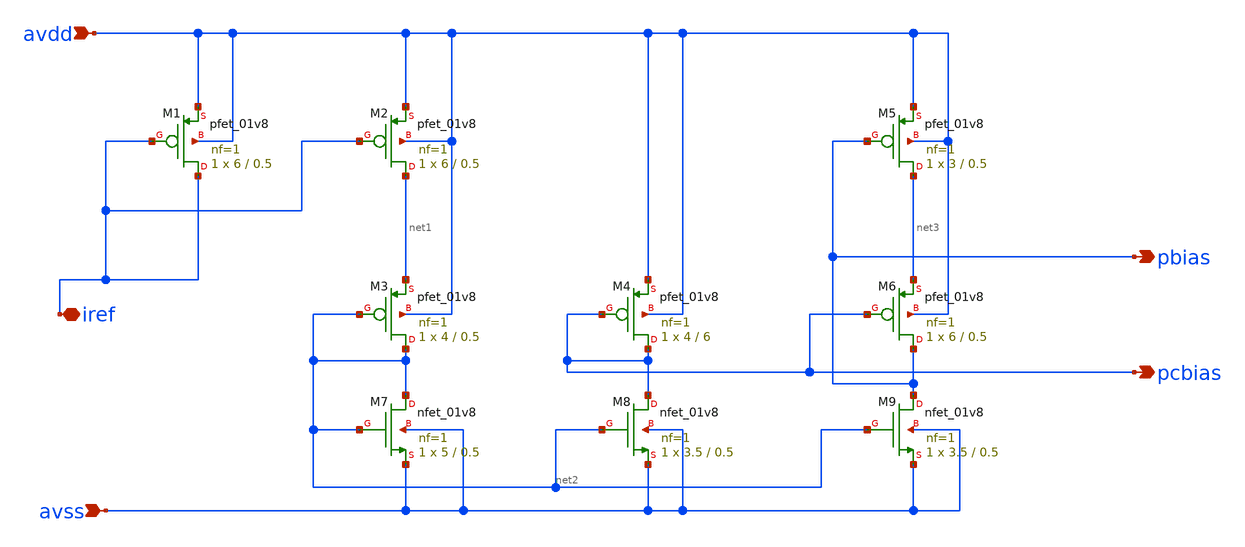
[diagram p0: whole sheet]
** sch_path: xsch/idac/p_ibias.sch
**.subckt p_ibias avdd avss iref pbias pcbias
*.ipin avdd
*.ipin avss
*.iopin iref
*.opin pbias
*.opin pcbias
XM1 iref iref avdd avdd sky130_fd_pr__pfet_01v8 L=0.5 W=6 nf=1 ad='int((nf+1)/2) * W/nf * 0.29' as='int((nf+2)/2) * W/nf * 0.29'
+ pd='2*int((nf+1)/2) * (W/nf + 0.29)' ps='2*int((nf+2)/2) * (W/nf + 0.29)' nrd='0.29 / W' nrs='0.29 / W'
+ sa=0 sb=0 sd=0 mult=1 m=1
XM2 net1 iref avdd avdd sky130_fd_pr__pfet_01v8 L=0.5 W=6 nf=1 ad='int((nf+1)/2) * W/nf * 0.29' as='int((nf+2)/2) * W/nf * 0.29'
+ pd='2*int((nf+1)/2) * (W/nf + 0.29)' ps='2*int((nf+2)/2) * (W/nf + 0.29)' nrd='0.29 / W' nrs='0.29 / W'
+ sa=0 sb=0 sd=0 mult=1 m=1
XM3 net2 net2 net1 avdd sky130_fd_pr__pfet_01v8 L=0.5 W=4 nf=1 ad='int((nf+1)/2) * W/nf * 0.29' as='int((nf+2)/2) * W/nf * 0.29'
+ pd='2*int((nf+1)/2) * (W/nf + 0.29)' ps='2*int((nf+2)/2) * (W/nf + 0.29)' nrd='0.29 / W' nrs='0.29 / W'
+ sa=0 sb=0 sd=0 mult=1 m=1
XM4 pcbias pcbias avdd avdd sky130_fd_pr__pfet_01v8 L=6 W=4 nf=1 ad='int((nf+1)/2) * W/nf * 0.29' as='int((nf+2)/2) * W/nf * 0.29'
+ pd='2*int((nf+1)/2) * (W/nf + 0.29)' ps='2*int((nf+2)/2) * (W/nf + 0.29)' nrd='0.29 / W' nrs='0.29 / W'
+ sa=0 sb=0 sd=0 mult=1 m=1
XM5 net3 pbias avdd avdd sky130_fd_pr__pfet_01v8 L=0.5 W=3 nf=1 ad='int((nf+1)/2) * W/nf * 0.29' as='int((nf+2)/2) * W/nf * 0.29'
+ pd='2*int((nf+1)/2) * (W/nf + 0.29)' ps='2*int((nf+2)/2) * (W/nf + 0.29)' nrd='0.29 / W' nrs='0.29 / W'
+ sa=0 sb=0 sd=0 mult=1 m=1
XM6 pbias pcbias net3 avdd sky130_fd_pr__pfet_01v8 L=0.5 W=6 nf=1 ad='int((nf+1)/2) * W/nf * 0.29' as='int((nf+2)/2) * W/nf * 0.29'
+ pd='2*int((nf+1)/2) * (W/nf + 0.29)' ps='2*int((nf+2)/2) * (W/nf + 0.29)' nrd='0.29 / W' nrs='0.29 / W'
+ sa=0 sb=0 sd=0 mult=1 m=1
XM7 net2 net2 avss avss sky130_fd_pr__nfet_01v8 L=0.5 W=5 nf=1 ad='int((nf+1)/2) * W/nf * 0.29' as='int((nf+2)/2) * W/nf * 0.29'
+ pd='2*int((nf+1)/2) * (W/nf + 0.29)' ps='2*int((nf+2)/2) * (W/nf + 0.29)' nrd='0.29 / W' nrs='0.29 / W'
+ sa=0 sb=0 sd=0 mult=1 m=1
XM8 pcbias net2 avss avss sky130_fd_pr__nfet_01v8 L=0.5 W=3.5 nf=1 ad='int((nf+1)/2) * W/nf * 0.29' as='int((nf+2)/2) * W/nf * 0.29'
+ pd='2*int((nf+1)/2) * (W/nf + 0.29)' ps='2*int((nf+2)/2) * (W/nf + 0.29)' nrd='0.29 / W' nrs='0.29 / W'
+ sa=0 sb=0 sd=0 mult=1 m=1
XM9 pbias net2 avss avss sky130_fd_pr__nfet_01v8 L=0.5 W=3.5 nf=1 ad='int((nf+1)/2) * W/nf * 0.29' as='int((nf+2)/2) * W/nf * 0.29'
+ pd='2*int((nf+1)/2) * (W/nf + 0.29)' ps='2*int((nf+2)/2) * (W/nf + 0.29)' nrd='0.29 / W' nrs='0.29 / W'
+ sa=0 sb=0 sd=0 mult=1 m=1
**.ends
.end
